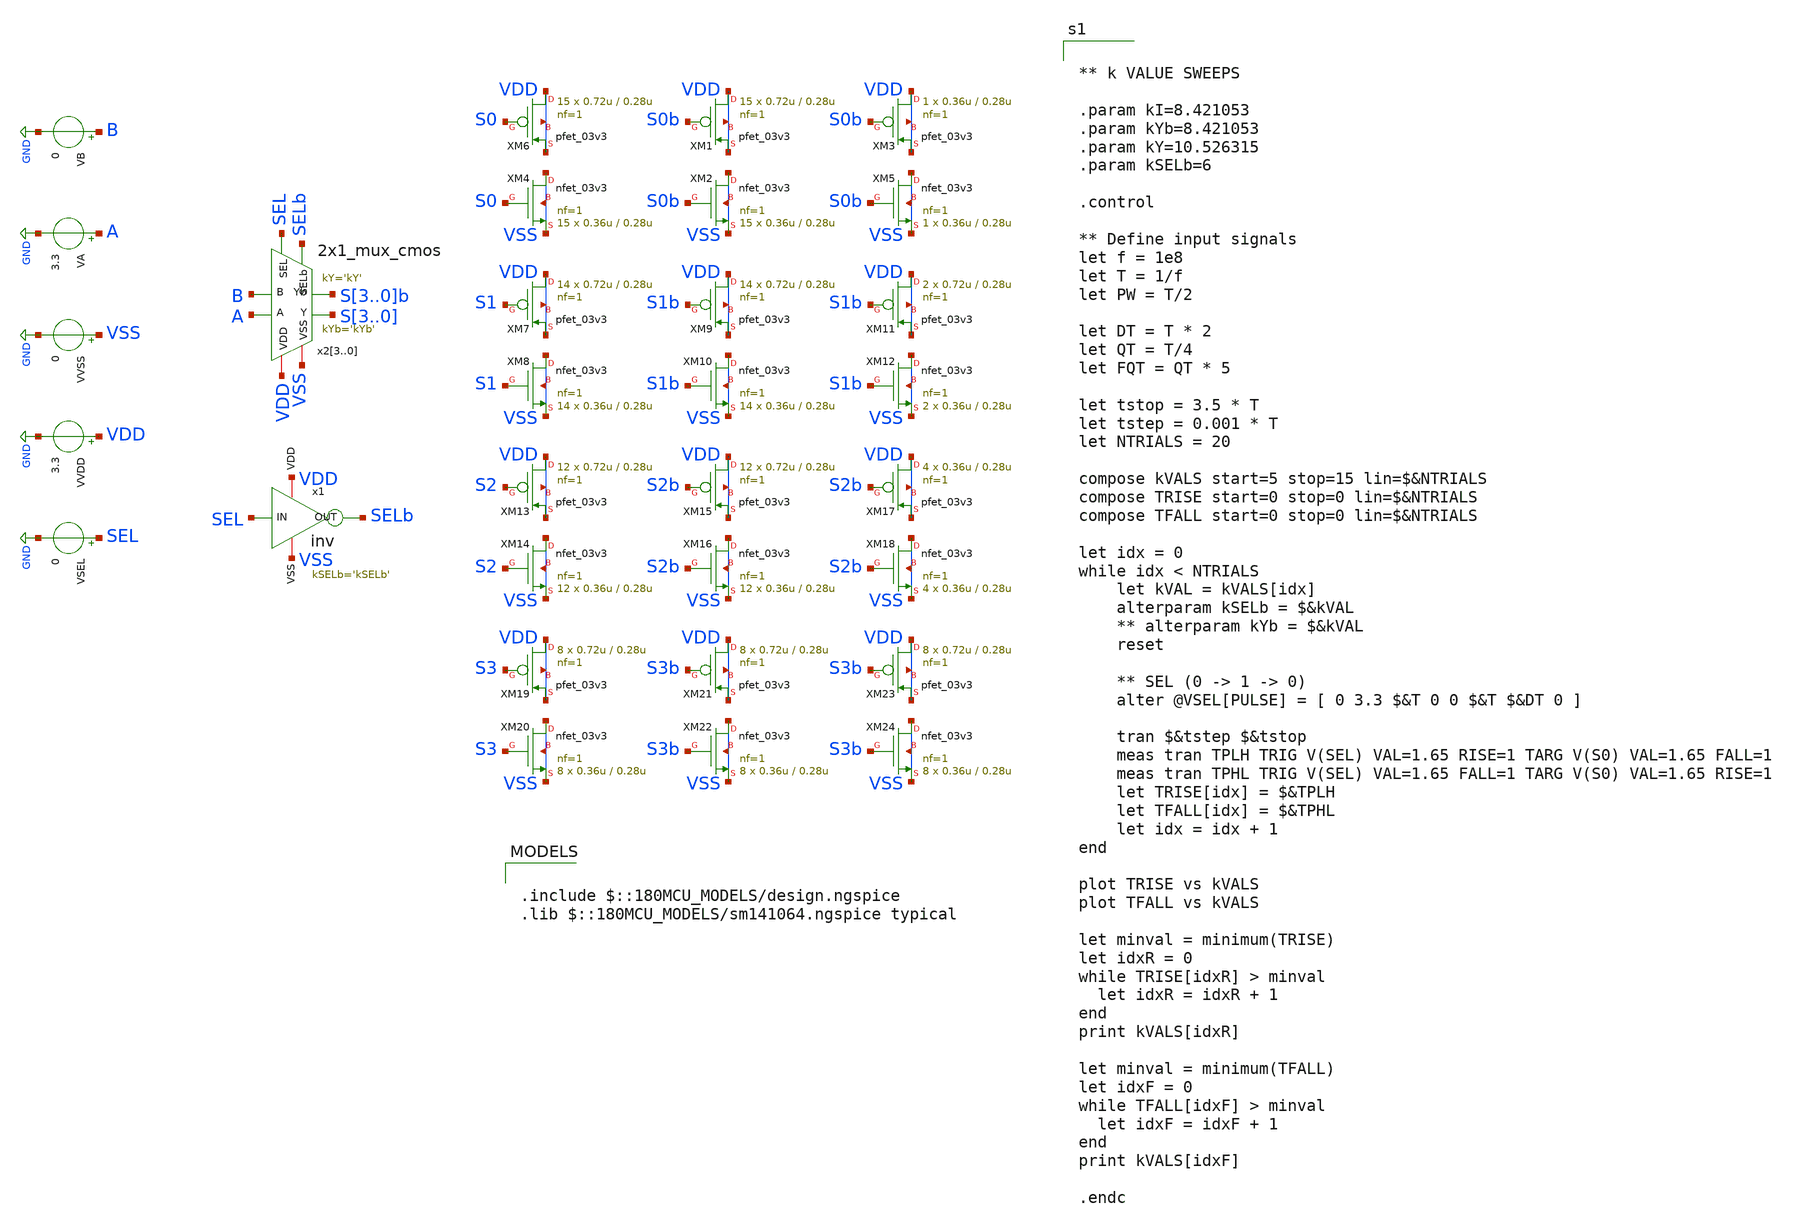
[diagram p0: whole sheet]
** sch_path: CAD5/shifter_sizing_tb.sch
**.subckt shifter_sizing_tb
x23 A SEL SELb S3 VDD VSS B S3b 2x1_mux_cmos kYb='kYb' kY='kY'
x22 A SEL SELb S2 VDD VSS B S2b 2x1_mux_cmos kYb='kYb' kY='kY'
x21 A SEL SELb S1 VDD VSS B S1b 2x1_mux_cmos kYb='kYb' kY='kY'
x20 A SEL SELb S0 VDD VSS B S0b 2x1_mux_cmos kYb='kYb' kY='kY'
x1 VDD SEL SELb VSS inv kSELb='kSELb'
XM6 VDD S0 VDD VDD pfet_03v3 L=0.28u W=0.72u nf=1 ad='int((nf+1)/2) * W/nf * 0.18u' as='int((nf+2)/2) * W/nf * 0.18u'
+ pd='2*int((nf+1)/2) * (W/nf + 0.18u)' ps='2*int((nf+2)/2) * (W/nf + 0.18u)' nrd='0.18u / W' nrs='0.18u / W'
+ sa=0 sb=0 sd=0 m=15
XM4 VSS S0 VSS VSS nfet_03v3 L=0.28u W=0.36u nf=1 ad='int((nf+1)/2) * W/nf * 0.18u' as='int((nf+2)/2) * W/nf * 0.18u'
+ pd='2*int((nf+1)/2) * (W/nf + 0.18u)' ps='2*int((nf+2)/2) * (W/nf + 0.18u)' nrd='0.18u / W' nrs='0.18u / W'
+ sa=0 sb=0 sd=0 m=15
XM1 VDD S0b VDD VDD pfet_03v3 L=0.28u W=0.72u nf=1 ad='int((nf+1)/2) * W/nf * 0.18u' as='int((nf+2)/2) * W/nf * 0.18u'
+ pd='2*int((nf+1)/2) * (W/nf + 0.18u)' ps='2*int((nf+2)/2) * (W/nf + 0.18u)' nrd='0.18u / W' nrs='0.18u / W'
+ sa=0 sb=0 sd=0 m=15
XM2 VSS S0b VSS VSS nfet_03v3 L=0.28u W=0.36u nf=1 ad='int((nf+1)/2) * W/nf * 0.18u' as='int((nf+2)/2) * W/nf * 0.18u'
+ pd='2*int((nf+1)/2) * (W/nf + 0.18u)' ps='2*int((nf+2)/2) * (W/nf + 0.18u)' nrd='0.18u / W' nrs='0.18u / W'
+ sa=0 sb=0 sd=0 m=15
XM3 VDD S0b VDD VDD pfet_03v3 L=0.28u W=0.36u nf=1 ad='int((nf+1)/2) * W/nf * 0.18u' as='int((nf+2)/2) * W/nf * 0.18u'
+ pd='2*int((nf+1)/2) * (W/nf + 0.18u)' ps='2*int((nf+2)/2) * (W/nf + 0.18u)' nrd='0.18u / W' nrs='0.18u / W'
+ sa=0 sb=0 sd=0 m=1
XM5 VSS S0b VSS VSS nfet_03v3 L=0.28u W=0.36u nf=1 ad='int((nf+1)/2) * W/nf * 0.18u' as='int((nf+2)/2) * W/nf * 0.18u'
+ pd='2*int((nf+1)/2) * (W/nf + 0.18u)' ps='2*int((nf+2)/2) * (W/nf + 0.18u)' nrd='0.18u / W' nrs='0.18u / W'
+ sa=0 sb=0 sd=0 m=1
XM7 VDD S1 VDD VDD pfet_03v3 L=0.28u W=0.72u nf=1 ad='int((nf+1)/2) * W/nf * 0.18u' as='int((nf+2)/2) * W/nf * 0.18u'
+ pd='2*int((nf+1)/2) * (W/nf + 0.18u)' ps='2*int((nf+2)/2) * (W/nf + 0.18u)' nrd='0.18u / W' nrs='0.18u / W'
+ sa=0 sb=0 sd=0 m=14
XM8 VSS S1 VSS VSS nfet_03v3 L=0.28u W=0.36u nf=1 ad='int((nf+1)/2) * W/nf * 0.18u' as='int((nf+2)/2) * W/nf * 0.18u'
+ pd='2*int((nf+1)/2) * (W/nf + 0.18u)' ps='2*int((nf+2)/2) * (W/nf + 0.18u)' nrd='0.18u / W' nrs='0.18u / W'
+ sa=0 sb=0 sd=0 m=14
XM9 VDD S1b VDD VDD pfet_03v3 L=0.28u W=0.72u nf=1 ad='int((nf+1)/2) * W/nf * 0.18u' as='int((nf+2)/2) * W/nf * 0.18u'
+ pd='2*int((nf+1)/2) * (W/nf + 0.18u)' ps='2*int((nf+2)/2) * (W/nf + 0.18u)' nrd='0.18u / W' nrs='0.18u / W'
+ sa=0 sb=0 sd=0 m=14
XM10 VSS S1b VSS VSS nfet_03v3 L=0.28u W=0.36u nf=1 ad='int((nf+1)/2) * W/nf * 0.18u' as='int((nf+2)/2) * W/nf * 0.18u'
+ pd='2*int((nf+1)/2) * (W/nf + 0.18u)' ps='2*int((nf+2)/2) * (W/nf + 0.18u)' nrd='0.18u / W' nrs='0.18u / W'
+ sa=0 sb=0 sd=0 m=14
XM11 VDD S1b VDD VDD pfet_03v3 L=0.28u W=0.72u nf=1 ad='int((nf+1)/2) * W/nf * 0.18u' as='int((nf+2)/2) * W/nf * 0.18u'
+ pd='2*int((nf+1)/2) * (W/nf + 0.18u)' ps='2*int((nf+2)/2) * (W/nf + 0.18u)' nrd='0.18u / W' nrs='0.18u / W'
+ sa=0 sb=0 sd=0 m=2
XM12 VSS S1b VSS VSS nfet_03v3 L=0.28u W=0.36u nf=1 ad='int((nf+1)/2) * W/nf * 0.18u' as='int((nf+2)/2) * W/nf * 0.18u'
+ pd='2*int((nf+1)/2) * (W/nf + 0.18u)' ps='2*int((nf+2)/2) * (W/nf + 0.18u)' nrd='0.18u / W' nrs='0.18u / W'
+ sa=0 sb=0 sd=0 m=2
XM13 VDD S2 VDD VDD pfet_03v3 L=0.28u W=0.72u nf=1 ad='int((nf+1)/2) * W/nf * 0.18u' as='int((nf+2)/2) * W/nf * 0.18u'
+ pd='2*int((nf+1)/2) * (W/nf + 0.18u)' ps='2*int((nf+2)/2) * (W/nf + 0.18u)' nrd='0.18u / W' nrs='0.18u / W'
+ sa=0 sb=0 sd=0 m=12
XM14 VSS S2 VSS VSS nfet_03v3 L=0.28u W=0.36u nf=1 ad='int((nf+1)/2) * W/nf * 0.18u' as='int((nf+2)/2) * W/nf * 0.18u'
+ pd='2*int((nf+1)/2) * (W/nf + 0.18u)' ps='2*int((nf+2)/2) * (W/nf + 0.18u)' nrd='0.18u / W' nrs='0.18u / W'
+ sa=0 sb=0 sd=0 m=12
XM15 VDD S2b VDD VDD pfet_03v3 L=0.28u W=0.72u nf=1 ad='int((nf+1)/2) * W/nf * 0.18u' as='int((nf+2)/2) * W/nf * 0.18u'
+ pd='2*int((nf+1)/2) * (W/nf + 0.18u)' ps='2*int((nf+2)/2) * (W/nf + 0.18u)' nrd='0.18u / W' nrs='0.18u / W'
+ sa=0 sb=0 sd=0 m=12
XM16 VSS S2b VSS VSS nfet_03v3 L=0.28u W=0.36u nf=1 ad='int((nf+1)/2) * W/nf * 0.18u' as='int((nf+2)/2) * W/nf * 0.18u'
+ pd='2*int((nf+1)/2) * (W/nf + 0.18u)' ps='2*int((nf+2)/2) * (W/nf + 0.18u)' nrd='0.18u / W' nrs='0.18u / W'
+ sa=0 sb=0 sd=0 m=12
XM17 VDD S2b VDD VDD pfet_03v3 L=0.28u W=0.36u nf=1 ad='int((nf+1)/2) * W/nf * 0.18u' as='int((nf+2)/2) * W/nf * 0.18u'
+ pd='2*int((nf+1)/2) * (W/nf + 0.18u)' ps='2*int((nf+2)/2) * (W/nf + 0.18u)' nrd='0.18u / W' nrs='0.18u / W'
+ sa=0 sb=0 sd=0 m=4
XM18 VSS S2b VSS VSS nfet_03v3 L=0.28u W=0.36u nf=1 ad='int((nf+1)/2) * W/nf * 0.18u' as='int((nf+2)/2) * W/nf * 0.18u'
+ pd='2*int((nf+1)/2) * (W/nf + 0.18u)' ps='2*int((nf+2)/2) * (W/nf + 0.18u)' nrd='0.18u / W' nrs='0.18u / W'
+ sa=0 sb=0 sd=0 m=4
XM19 VDD S3 VDD VDD pfet_03v3 L=0.28u W=0.72u nf=1 ad='int((nf+1)/2) * W/nf * 0.18u' as='int((nf+2)/2) * W/nf * 0.18u'
+ pd='2*int((nf+1)/2) * (W/nf + 0.18u)' ps='2*int((nf+2)/2) * (W/nf + 0.18u)' nrd='0.18u / W' nrs='0.18u / W'
+ sa=0 sb=0 sd=0 m=8
XM20 VSS S3 VSS VSS nfet_03v3 L=0.28u W=0.36u nf=1 ad='int((nf+1)/2) * W/nf * 0.18u' as='int((nf+2)/2) * W/nf * 0.18u'
+ pd='2*int((nf+1)/2) * (W/nf + 0.18u)' ps='2*int((nf+2)/2) * (W/nf + 0.18u)' nrd='0.18u / W' nrs='0.18u / W'
+ sa=0 sb=0 sd=0 m=8
XM21 VDD S3b VDD VDD pfet_03v3 L=0.28u W=0.72u nf=1 ad='int((nf+1)/2) * W/nf * 0.18u' as='int((nf+2)/2) * W/nf * 0.18u'
+ pd='2*int((nf+1)/2) * (W/nf + 0.18u)' ps='2*int((nf+2)/2) * (W/nf + 0.18u)' nrd='0.18u / W' nrs='0.18u / W'
+ sa=0 sb=0 sd=0 m=8
XM22 VSS S3b VSS VSS nfet_03v3 L=0.28u W=0.36u nf=1 ad='int((nf+1)/2) * W/nf * 0.18u' as='int((nf+2)/2) * W/nf * 0.18u'
+ pd='2*int((nf+1)/2) * (W/nf + 0.18u)' ps='2*int((nf+2)/2) * (W/nf + 0.18u)' nrd='0.18u / W' nrs='0.18u / W'
+ sa=0 sb=0 sd=0 m=8
XM23 VDD S3b VDD VDD pfet_03v3 L=0.28u W=0.72u nf=1 ad='int((nf+1)/2) * W/nf * 0.18u' as='int((nf+2)/2) * W/nf * 0.18u'
+ pd='2*int((nf+1)/2) * (W/nf + 0.18u)' ps='2*int((nf+2)/2) * (W/nf + 0.18u)' nrd='0.18u / W' nrs='0.18u / W'
+ sa=0 sb=0 sd=0 m=8
XM24 VSS S3b VSS VSS nfet_03v3 L=0.28u W=0.36u nf=1 ad='int((nf+1)/2) * W/nf * 0.18u' as='int((nf+2)/2) * W/nf * 0.18u'
+ pd='2*int((nf+1)/2) * (W/nf + 0.18u)' ps='2*int((nf+2)/2) * (W/nf + 0.18u)' nrd='0.18u / W' nrs='0.18u / W'
+ sa=0 sb=0 sd=0 m=8
VVDD VDD GND 3.3
VVSS VSS GND 0
VSEL SEL GND 0
VA A GND 3.3
VB B GND 0
**** begin user architecture code

.include $::180MCU_MODELS/design.ngspice
.lib $::180MCU_MODELS/sm141064.ngspice typical



** k VALUE SWEEPS

.param kI=8.421053
.param kYb=8.421053
.param kY=10.526315
.param kSELb=6

.control

** Define input signals
let f = 1e8
let T = 1/f
let PW = T/2

let DT = T * 2
let QT = T/4
let FQT = QT * 5

let tstop = 3.5 * T
let tstep = 0.001 * T
let NTRIALS = 20

compose kVALS start=5 stop=15 lin=$&NTRIALS
compose TRISE start=0 stop=0 lin=$&NTRIALS
compose TFALL start=0 stop=0 lin=$&NTRIALS

let idx = 0
while idx < NTRIALS
	let kVAL = kVALS[idx]
	alterparam kSELb = $&kVAL
    ** alterparam kYb = $&kVAL
	reset

    ** SEL (0 -> 1 -> 0)
    alter @VSEL[PULSE] = [ 0 3.3 $&T 0 0 $&T $&DT 0 ]

	tran $&tstep $&tstop
	meas tran TPLH TRIG V(SEL) VAL=1.65 RISE=1 TARG V(S0) VAL=1.65 FALL=1
    meas tran TPHL TRIG V(SEL) VAL=1.65 FALL=1 TARG V(S0) VAL=1.65 RISE=1
	let TRISE[idx] = $&TPLH
	let TFALL[idx] = $&TPHL
	let idx = idx + 1
end

plot TRISE vs kVALS
plot TFALL vs kVALS

let minval = minimum(TRISE)
let idxR = 0
while TRISE[idxR] > minval
  let idxR = idxR + 1
end
print kVALS[idxR]

let minval = minimum(TFALL)
let idxF = 0
while TFALL[idxF] > minval
  let idxF = idxF + 1
end
print kVALS[idxF]

.endc


**** end user architecture code
**.ends

* expanding   symbol:  engn1600-team1/CAD5/2x1_mux_cmos.sym # of pins=8
** sym_path: CAD4/2x1_mux_cmos.sym
** sch_path: CAD4/2x1_mux_cmos.sch
.subckt 2x1_mux_cmos A SEL SELb Y VDD VSS B Yb  kYb=1 kY=1
*.ipin A
*.ipin B
*.ipin SEL
*.opin Y
*.iopin VDD
*.iopin VSS
*.ipin SELb
*.opin Yb
XM1 VSS B net1 VSS nfet_03v3 L=0.28u W='kI*0.36u' nf=1 ad='int((nf+1)/2) * W/nf * 0.18u' as='int((nf+2)/2) * W/nf * 0.18u'
+ pd='2*int((nf+1)/2) * (W/nf + 0.18u)' ps='2*int((nf+2)/2) * (W/nf + 0.18u)' nrd='0.18u / W' nrs='0.18u / W'
+ sa=0 sb=0 sd=0 m=1
XM2 net1 SEL Yb VSS nfet_03v3 L=0.28u W='kYb*0.36u' nf=1 ad='int((nf+1)/2) * W/nf * 0.18u' as='int((nf+2)/2) * W/nf * 0.18u'
+ pd='2*int((nf+1)/2) * (W/nf + 0.18u)' ps='2*int((nf+2)/2) * (W/nf + 0.18u)' nrd='0.18u / W' nrs='0.18u / W'
+ sa=0 sb=0 sd=0 m=1
XM3 Yb SELb net2 VSS nfet_03v3 L=0.28u W='kYb*0.36u' nf=1 ad='int((nf+1)/2) * W/nf * 0.18u' as='int((nf+2)/2) * W/nf * 0.18u'
+ pd='2*int((nf+1)/2) * (W/nf + 0.18u)' ps='2*int((nf+2)/2) * (W/nf + 0.18u)' nrd='0.18u / W' nrs='0.18u / W'
+ sa=0 sb=0 sd=0 m=1
XM4 net2 A VSS VSS nfet_03v3 L=0.28u W='kI*0.36u' nf=1 ad='int((nf+1)/2) * W/nf * 0.18u' as='int((nf+2)/2) * W/nf * 0.18u'
+ pd='2*int((nf+1)/2) * (W/nf + 0.18u)' ps='2*int((nf+2)/2) * (W/nf + 0.18u)' nrd='0.18u / W' nrs='0.18u / W'
+ sa=0 sb=0 sd=0 m=1
XM5 net3 SELb Yb VDD pfet_03v3 L=0.28u W='kYb*0.72u' nf=1 ad='int((nf+1)/2) * W/nf * 0.18u' as='int((nf+2)/2) * W/nf * 0.18u'
+ pd='2*int((nf+1)/2) * (W/nf + 0.18u)' ps='2*int((nf+2)/2) * (W/nf + 0.18u)' nrd='0.18u / W' nrs='0.18u / W'
+ sa=0 sb=0 sd=0 m=1
XM6 VDD B net3 VDD pfet_03v3 L=0.28u W='kI*0.72u' nf=1 ad='int((nf+1)/2) * W/nf * 0.18u' as='int((nf+2)/2) * W/nf * 0.18u'
+ pd='2*int((nf+1)/2) * (W/nf + 0.18u)' ps='2*int((nf+2)/2) * (W/nf + 0.18u)' nrd='0.18u / W' nrs='0.18u / W'
+ sa=0 sb=0 sd=0 m=1
XM7 net4 A VDD VDD pfet_03v3 L=0.28u W='kI*0.72u' nf=1 ad='int((nf+1)/2) * W/nf * 0.18u' as='int((nf+2)/2) * W/nf * 0.18u'
+ pd='2*int((nf+1)/2) * (W/nf + 0.18u)' ps='2*int((nf+2)/2) * (W/nf + 0.18u)' nrd='0.18u / W' nrs='0.18u / W'
+ sa=0 sb=0 sd=0 m=1
XM8 Yb SEL net4 VDD pfet_03v3 L=0.28u W='kYb*0.72u' nf=1 ad='int((nf+1)/2) * W/nf * 0.18u' as='int((nf+2)/2) * W/nf * 0.18u'
+ pd='2*int((nf+1)/2) * (W/nf + 0.18u)' ps='2*int((nf+2)/2) * (W/nf + 0.18u)' nrd='0.18u / W' nrs='0.18u / W'
+ sa=0 sb=0 sd=0 m=1
XM9 VSS Yb Y VSS nfet_03v3 L=0.28u W='kY*0.36u' nf=1 ad='int((nf+1)/2) * W/nf * 0.18u' as='int((nf+2)/2) * W/nf * 0.18u'
+ pd='2*int((nf+1)/2) * (W/nf + 0.18u)' ps='2*int((nf+2)/2) * (W/nf + 0.18u)' nrd='0.18u / W' nrs='0.18u / W'
+ sa=0 sb=0 sd=0 m=1
XM10 VDD Yb Y VDD pfet_03v3 L=0.28u W='kY*0.72u' nf=1 ad='int((nf+1)/2) * W/nf * 0.18u' as='int((nf+2)/2) * W/nf * 0.18u'
+ pd='2*int((nf+1)/2) * (W/nf + 0.18u)' ps='2*int((nf+2)/2) * (W/nf + 0.18u)' nrd='0.18u / W' nrs='0.18u / W'
+ sa=0 sb=0 sd=0 m=1
**** begin user architecture code


.param kI=2.5
.param kYb=1.875
.param kY=2.1527777777777778


**** end user architecture code
.ends


* expanding   symbol:  engn1600-team1/CAD5/inv.sym # of pins=4
** sym_path: CAD5/inv.sym
** sch_path: CAD5/inv.sch
.subckt inv VDD IN OUT VSS  kSELb=1
*.ipin IN
*.opin OUT
*.iopin VDD
*.iopin VSS
XM1 OUT IN VDD VDD pfet_03v3 L=0.28u W='kSELb*0.72u' nf=1 ad='int((nf+1)/2) * W/nf * 0.18u' as='int((nf+2)/2) * W/nf * 0.18u'
+ pd='2*int((nf+1)/2) * (W/nf + 0.18u)' ps='2*int((nf+2)/2) * (W/nf + 0.18u)' nrd='0.18u / W' nrs='0.18u / W'
+ sa=0 sb=0 sd=0 m=1
XM2 OUT IN VSS VSS nfet_03v3 L=0.28u W='kSELb*0.36u' nf=1 ad='int((nf+1)/2) * W/nf * 0.18u' as='int((nf+2)/2) * W/nf * 0.18u'
+ pd='2*int((nf+1)/2) * (W/nf + 0.18u)' ps='2*int((nf+2)/2) * (W/nf + 0.18u)' nrd='0.18u / W' nrs='0.18u / W'
+ sa=0 sb=0 sd=0 m=1
**** begin user architecture code


.param kSELb=1


**** end user architecture code
.ends

.GLOBAL GND
.end
